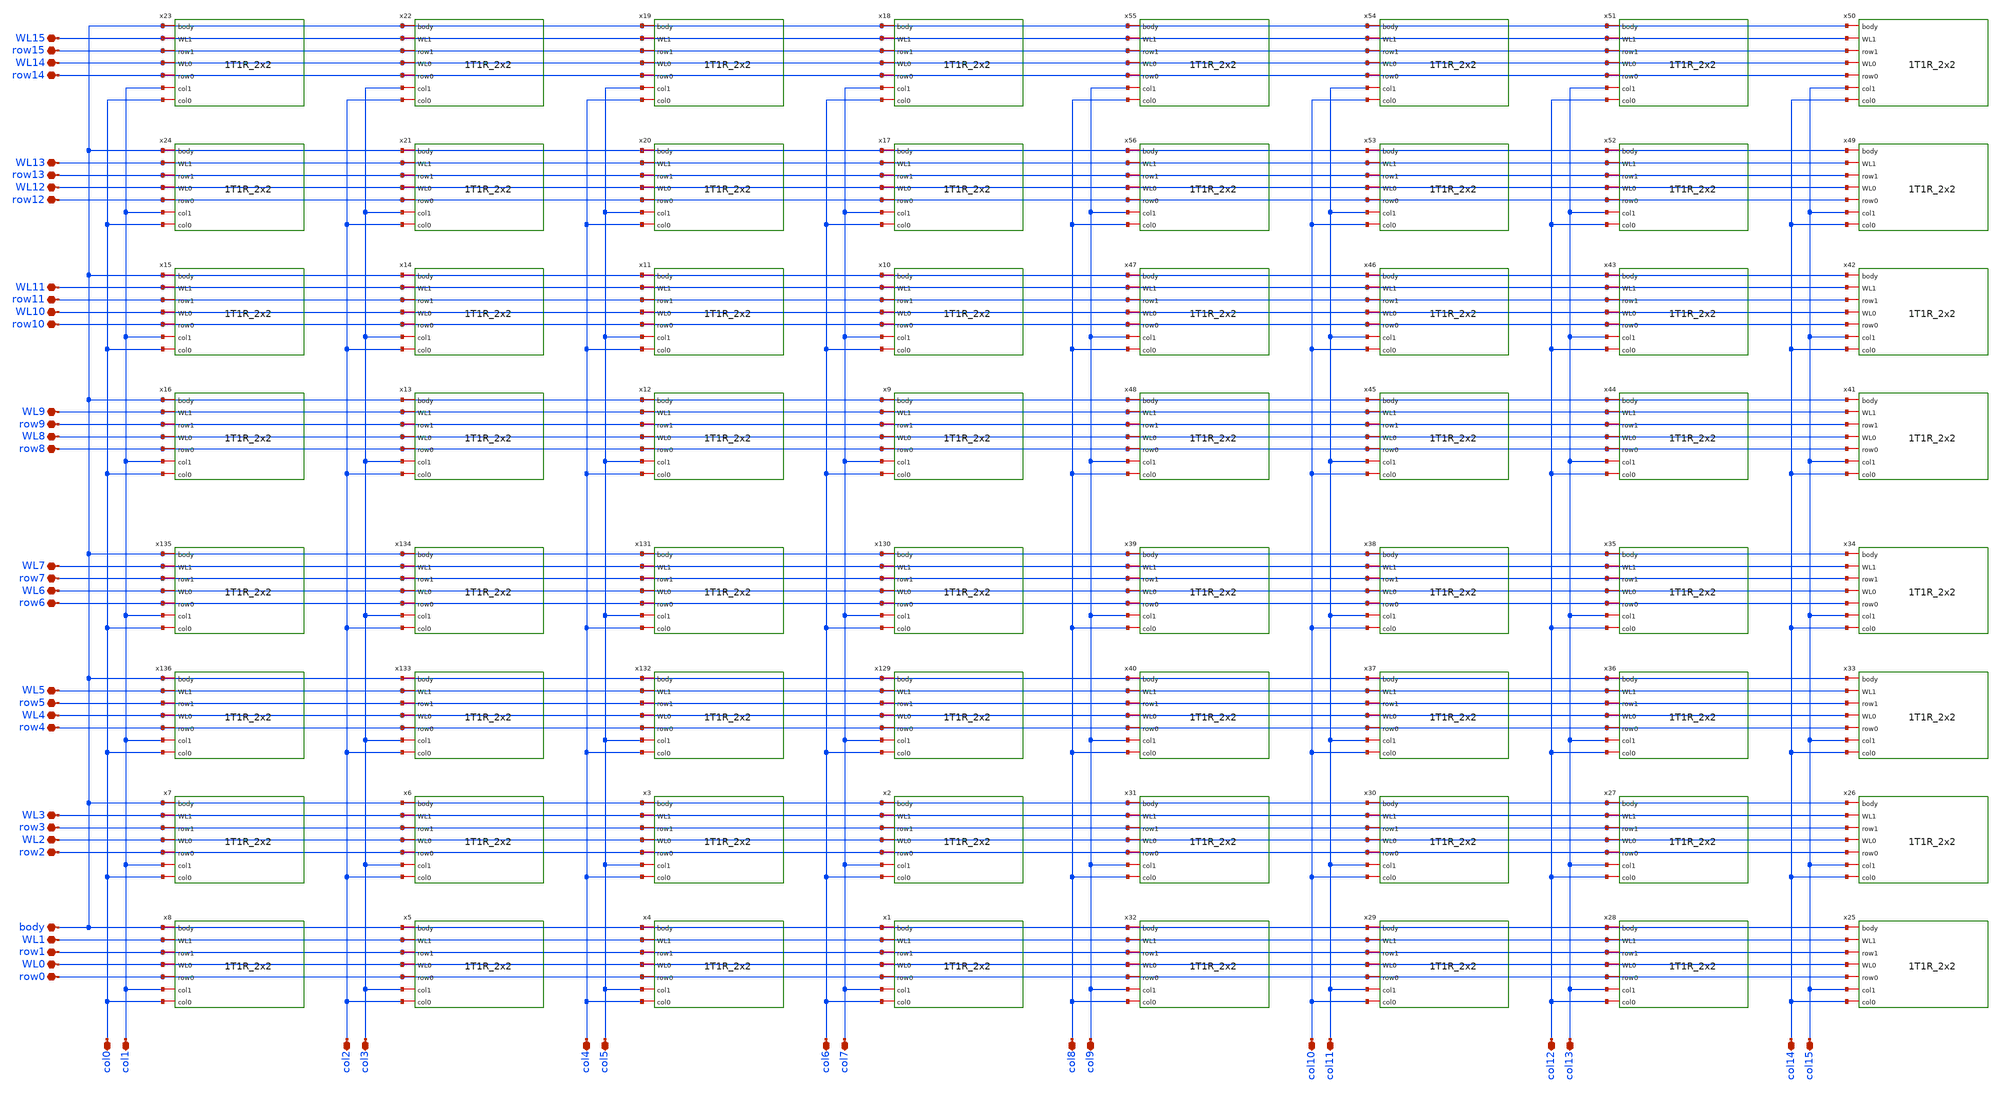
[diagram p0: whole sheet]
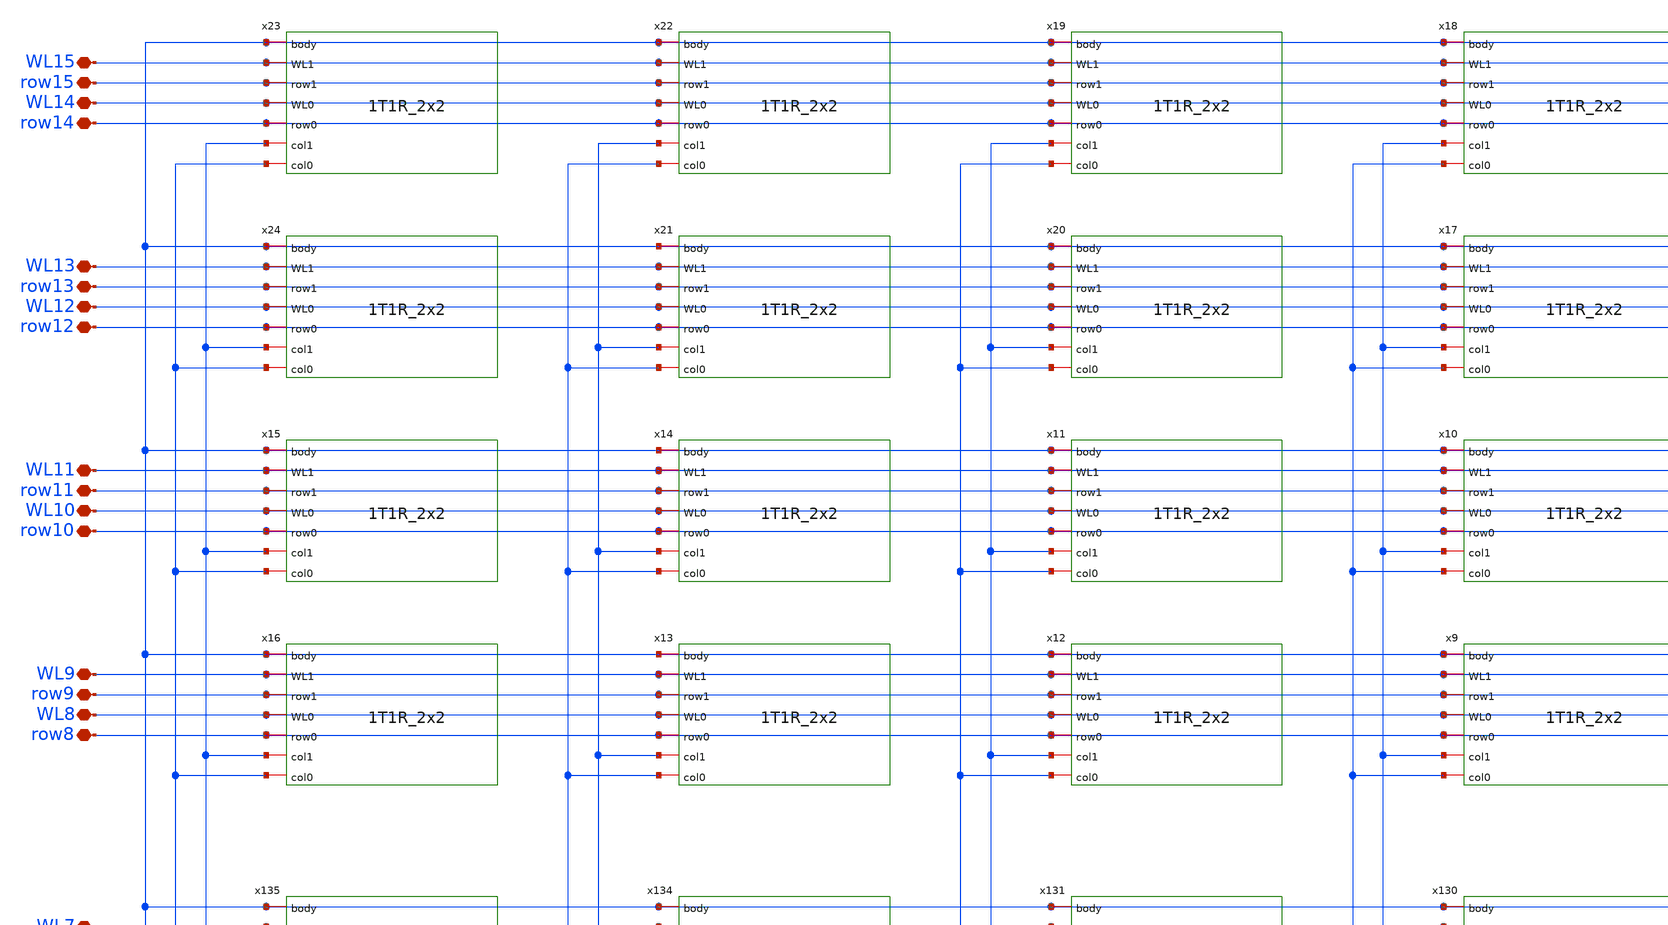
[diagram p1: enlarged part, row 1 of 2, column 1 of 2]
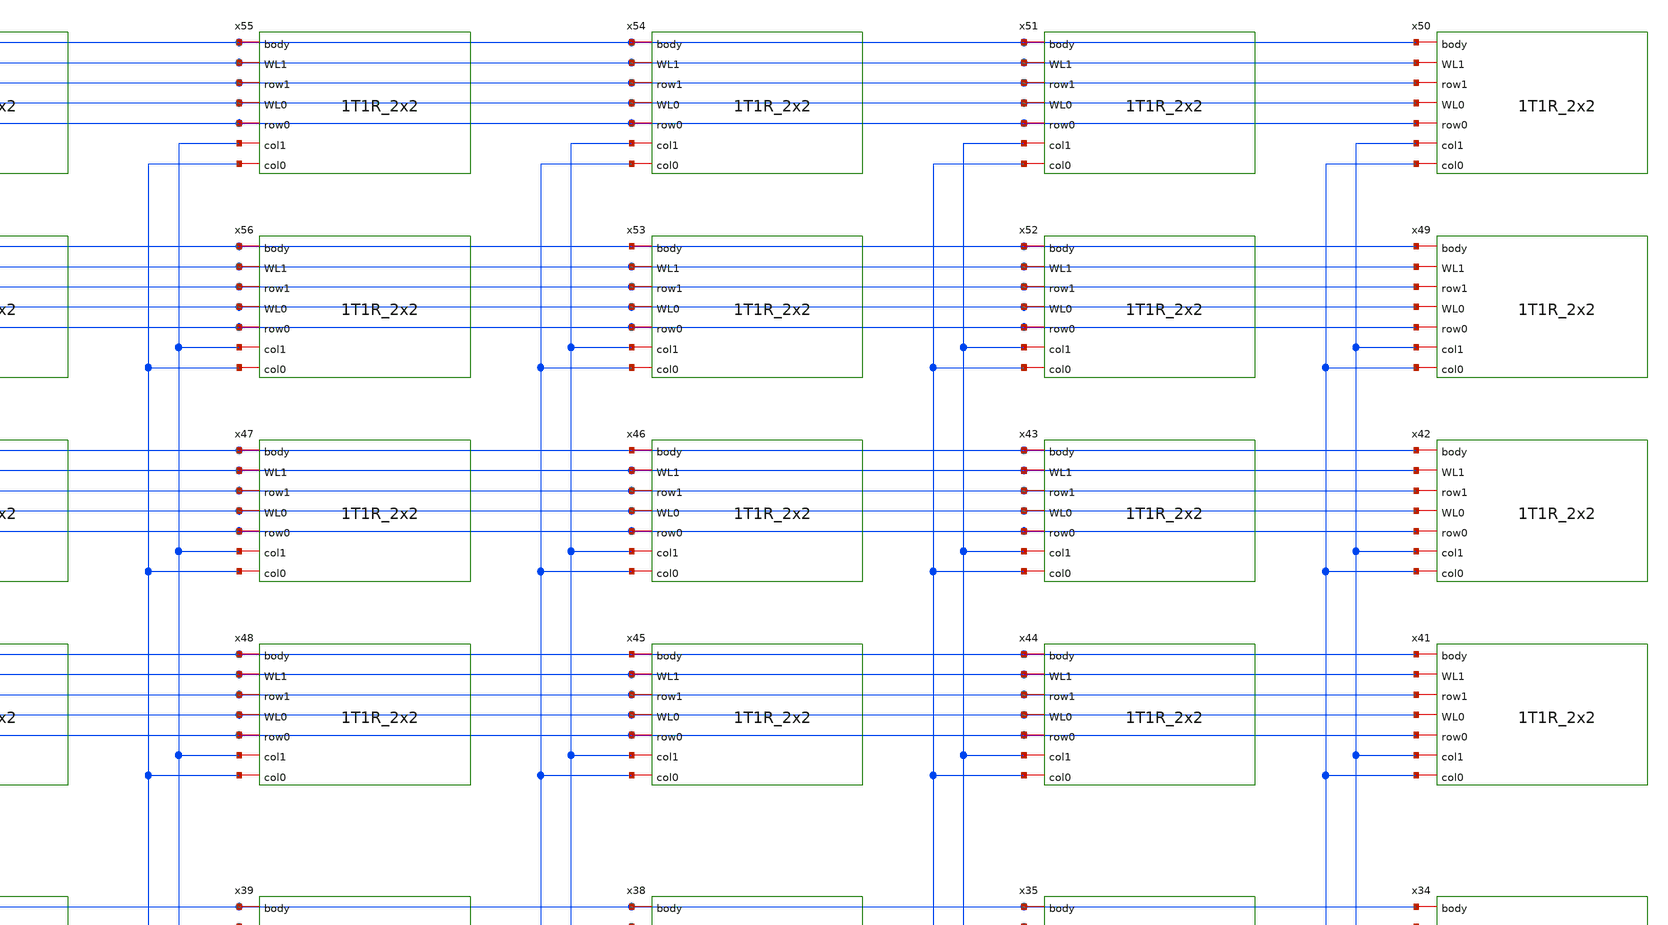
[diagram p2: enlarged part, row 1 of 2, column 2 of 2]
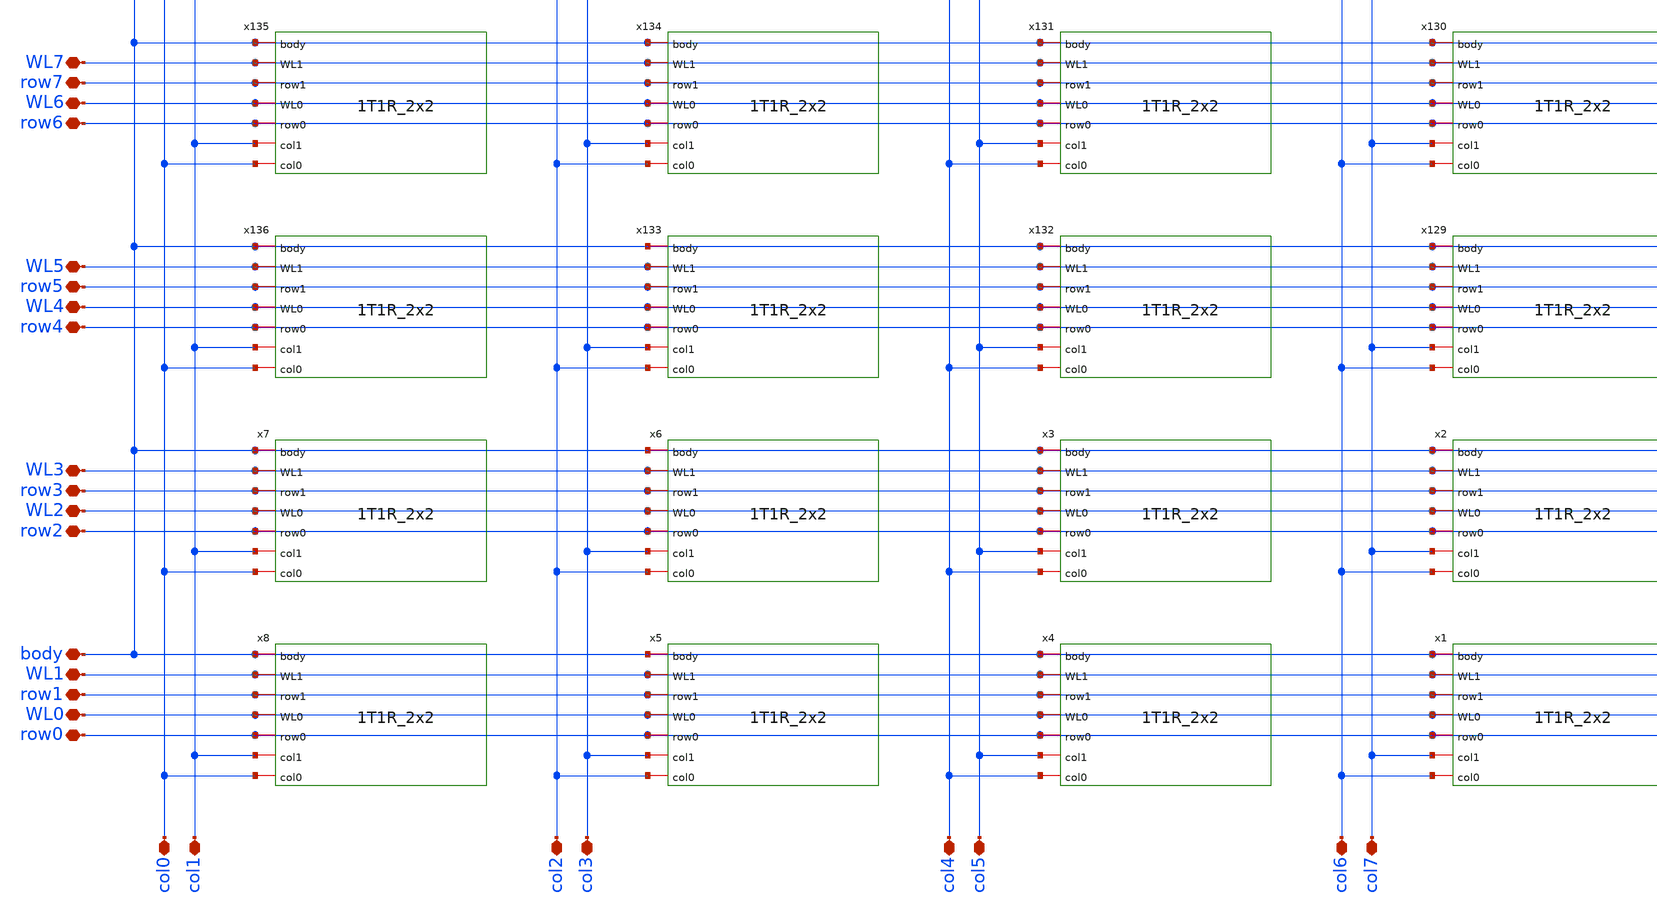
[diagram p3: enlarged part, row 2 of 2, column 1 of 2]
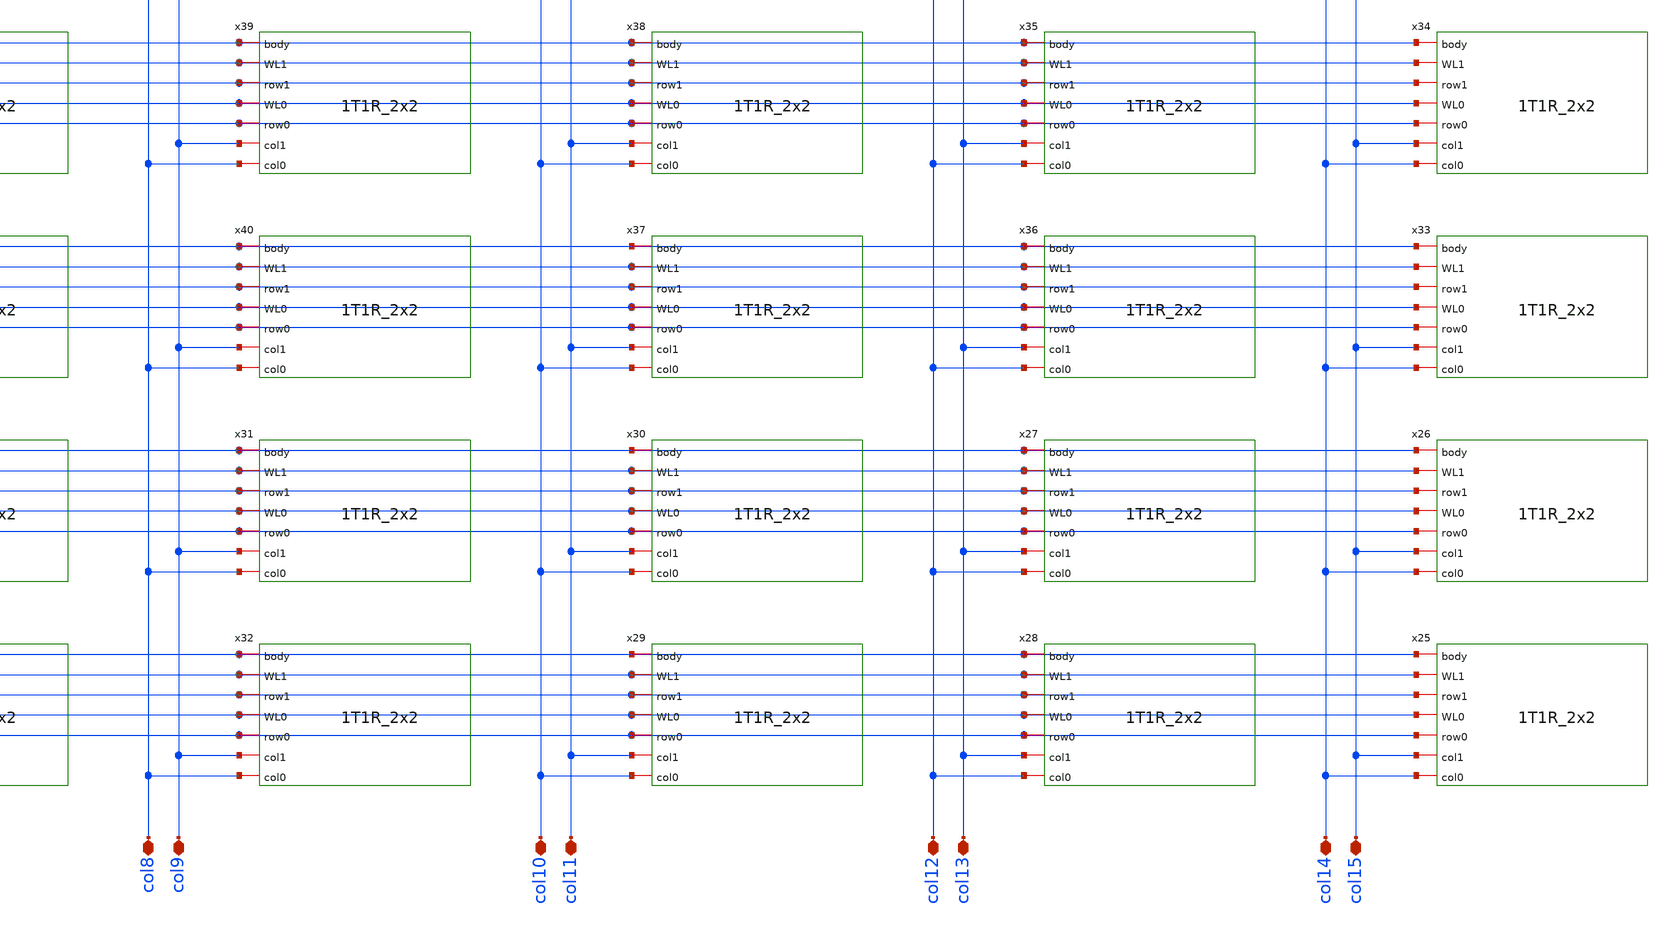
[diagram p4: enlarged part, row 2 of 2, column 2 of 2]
** sch_path: xschem/1T1R_16x16.sch
* StefanSchippers/xschem_sky130/sky130_fd_pr/reram.sym:
* Copyright 2021 Stefan Frederik Schippers
* Licensed under the Apache License, Version 2.0 (the "License");
**.subckt 1T1R_16x16 row0 WL0 row1 WL1 body row2 WL2 row3 WL3 row4 WL4 row5 WL5 row6 WL6 row7 WL7
*+ col1 col0 col3 col2 col5 col4 col7 col6 row8 WL8 row9 WL9 row10 WL10 row11 WL11 row12 WL12 row13 WL13
*+ row14 WL14 row15 WL15 col9 col8 col11 col10 col13 col12 col15 col14
*.iopin row0
*.iopin WL0
*.iopin row1
*.iopin WL1
*.iopin body
*.iopin row2
*.iopin WL2
*.iopin row3
*.iopin WL3
*.iopin row4
*.iopin WL4
*.iopin row5
*.iopin WL5
*.iopin row6
*.iopin WL6
*.iopin row7
*.iopin WL7
*.iopin col1
*.iopin col0
*.iopin col3
*.iopin col2
*.iopin col5
*.iopin col4
*.iopin col7
*.iopin col6
*.iopin row8
*.iopin WL8
*.iopin row9
*.iopin WL9
*.iopin row10
*.iopin WL10
*.iopin row11
*.iopin WL11
*.iopin row12
*.iopin WL12
*.iopin row13
*.iopin WL13
*.iopin row14
*.iopin WL14
*.iopin row15
*.iopin WL15
*.iopin col9
*.iopin col8
*.iopin col11
*.iopin col10
*.iopin col13
*.iopin col12
*.iopin col15
*.iopin col14
x1 body WL1 row1 WL0 row0 col7 col6 1T1R_2x2
x2 body WL3 row3 WL2 row2 col7 col6 1T1R_2x2
x3 body WL3 row3 WL2 row2 col5 col4 1T1R_2x2
x4 body WL1 row1 WL0 row0 col5 col4 1T1R_2x2
x5 body WL1 row1 WL0 row0 col3 col2 1T1R_2x2
x6 body WL3 row3 WL2 row2 col3 col2 1T1R_2x2
x7 body WL3 row3 WL2 row2 col1 col0 1T1R_2x2
x8 body WL1 row1 WL0 row0 col1 col0 1T1R_2x2
x129 body WL5 row5 WL4 row4 col7 col6 1T1R_2x2
x130 body WL7 row7 WL6 row6 col7 col6 1T1R_2x2
x131 body WL7 row7 WL6 row6 col5 col4 1T1R_2x2
x132 body WL5 row5 WL4 row4 col5 col4 1T1R_2x2
x133 body WL5 row5 WL4 row4 col3 col2 1T1R_2x2
x134 body WL7 row7 WL6 row6 col3 col2 1T1R_2x2
x135 body WL7 row7 WL6 row6 col1 col0 1T1R_2x2
x136 body WL5 row5 WL4 row4 col1 col0 1T1R_2x2
x9 body WL9 row9 WL8 row8 col7 col6 1T1R_2x2
x10 body WL11 row11 WL10 row10 col7 col6 1T1R_2x2
x11 body WL11 row11 WL10 row10 col5 col4 1T1R_2x2
x12 body WL9 row9 WL8 row8 col5 col4 1T1R_2x2
x13 body WL9 row9 WL8 row8 col3 col2 1T1R_2x2
x14 body WL11 row11 WL10 row10 col3 col2 1T1R_2x2
x15 body WL11 row11 WL10 row10 col1 col0 1T1R_2x2
x16 body WL9 row9 WL8 row8 col1 col0 1T1R_2x2
x17 body WL13 row13 WL12 row12 col7 col6 1T1R_2x2
x18 body WL15 row15 WL14 row14 col7 col6 1T1R_2x2
x19 body WL15 row15 WL14 row14 col5 col4 1T1R_2x2
x20 body WL13 row13 WL12 row12 col5 col4 1T1R_2x2
x21 body WL13 row13 WL12 row12 col3 col2 1T1R_2x2
x22 body WL15 row15 WL14 row14 col3 col2 1T1R_2x2
x23 body WL15 row15 WL14 row14 col1 col0 1T1R_2x2
x24 body WL13 row13 WL12 row12 col1 col0 1T1R_2x2
x25 body WL1 row1 WL0 row0 col15 col14 1T1R_2x2
x26 body WL3 row3 WL2 row2 col15 col14 1T1R_2x2
x27 body WL3 row3 WL2 row2 col13 col12 1T1R_2x2
x28 body WL1 row1 WL0 row0 col13 col12 1T1R_2x2
x29 body WL1 row1 WL0 row0 col11 col10 1T1R_2x2
x30 body WL3 row3 WL2 row2 col11 col10 1T1R_2x2
x31 body WL3 row3 WL2 row2 col9 col8 1T1R_2x2
x32 body WL1 row1 WL0 row0 col9 col8 1T1R_2x2
x33 body WL5 row5 WL4 row4 col15 col14 1T1R_2x2
x34 body WL7 row7 WL6 row6 col15 col14 1T1R_2x2
x35 body WL7 row7 WL6 row6 col13 col12 1T1R_2x2
x36 body WL5 row5 WL4 row4 col13 col12 1T1R_2x2
x37 body WL5 row5 WL4 row4 col11 col10 1T1R_2x2
x38 body WL7 row7 WL6 row6 col11 col10 1T1R_2x2
x39 body WL7 row7 WL6 row6 col9 col8 1T1R_2x2
x40 body WL5 row5 WL4 row4 col9 col8 1T1R_2x2
x41 body WL9 row9 WL8 row8 col15 col14 1T1R_2x2
x42 body WL11 row11 WL10 row10 col15 col14 1T1R_2x2
x43 body WL11 row11 WL10 row10 col13 col12 1T1R_2x2
x44 body WL9 row9 WL8 row8 col13 col12 1T1R_2x2
x45 body WL9 row9 WL8 row8 col11 col10 1T1R_2x2
x46 body WL11 row11 WL10 row10 col11 col10 1T1R_2x2
x47 body WL11 row11 WL10 row10 col9 col8 1T1R_2x2
x48 body WL9 row9 WL8 row8 col9 col8 1T1R_2x2
x49 body WL13 row13 WL12 row12 col15 col14 1T1R_2x2
x50 body WL15 row15 WL14 row14 col15 col14 1T1R_2x2
x51 body WL15 row15 WL14 row14 col13 col12 1T1R_2x2
x52 body WL13 row13 WL12 row12 col13 col12 1T1R_2x2
x53 body WL13 row13 WL12 row12 col11 col10 1T1R_2x2
x54 body WL15 row15 WL14 row14 col11 col10 1T1R_2x2
x55 body WL15 row15 WL14 row14 col9 col8 1T1R_2x2
x56 body WL13 row13 WL12 row12 col9 col8 1T1R_2x2
**.ends

* expanding   symbol:  /Volumes/export/isn/soumil/ReRAM_sky130_files/1T1R_2x2.sym # of pins=7
** sym_path: xschem/1T1R_2x2.sym
** sch_path: xschem/1T1R_2x2.sch
.subckt 1T1R_2x2 body WL1 row1 WL0 row0 col1 col0
*.iopin row1
*.iopin WL1
*.iopin row0
*.iopin WL0
*.iopin body
*.iopin col0
*.iopin col1
X1 row1 WL1 body col1 1T1R
X2 row0 WL0 body col1 1T1R
X3 row0 WL0 body col0 1T1R
X4 row1 WL1 body col0 1T1R
.ends


* expanding   symbol:  /Volumes/export/isn/soumil/ReRAM_sky130_files/1T1R.sym # of pins=4
** sym_path: xschem/1T1R.sym
** sch_path: xschem/1T1R.sch
.subckt 1T1R row WL body col
*.iopin WL
*.iopin body
*.iopin row
*.iopin col
XM1 net1 WL col body sky130_fd_pr__nfet_g5v0d10v5 L=0.5 W=1 nf=1 ad='int((nf+1)/2) * W/nf * 0.29' as='int((nf+2)/2) * W/nf * 0.29'
+ pd='2*int((nf+1)/2) * (W/nf + 0.29)' ps='2*int((nf+2)/2) * (W/nf + 0.29)' nrd='0.29 / W' nrs='0.29 / W'
+ sa=0 sb=0 sd=0 mult=1 m=1
XR1 row net1 reram_reram_cell Tfilament_0=3.8e-9
.ends

**** begin user architecture code

.subckt sky130_fd_pr_reram__reram_cell TE BE Tfilament_0=3.3e-9 area_ox=0.1024e-12
N1 TE BE nFilament sky130_fd_pr_reram__reram_model
.ic v(nFilament)={Tfilament_0*1.0e9}
.ends sky130_fd_pr_reram__reram_cell

.model sky130_fd_pr_reram__reram_model sky130_fd_pr_reram__reram_module  area_ox = 0.1024e-12  Tox =
+ 5.0  Tfilament_max = 4.9  Tfilament_min = 3.3  Eact_generation = 1.501  Eact_recombination  = 1.500
+  I_k1  = 6.140e-5  Tfilament_ref = 4.7249  V_ref = 0.430  velocity_k1 = 150  gamma_k0  = 16.5  gamma_k1
+  = -1.25  Temperature_0 = 300  C_thermal = 3.1825e-16  tau_thermal = 0.23e-9  t_step  = 1.0e-9
+  smoothing = 1e-7  Kclip = 200

.control
pre_osdi $SKYWATER_MODELS/sky130_fd_pr_reram__reram_module.osdi
.endc

**** end user architecture code
.end
